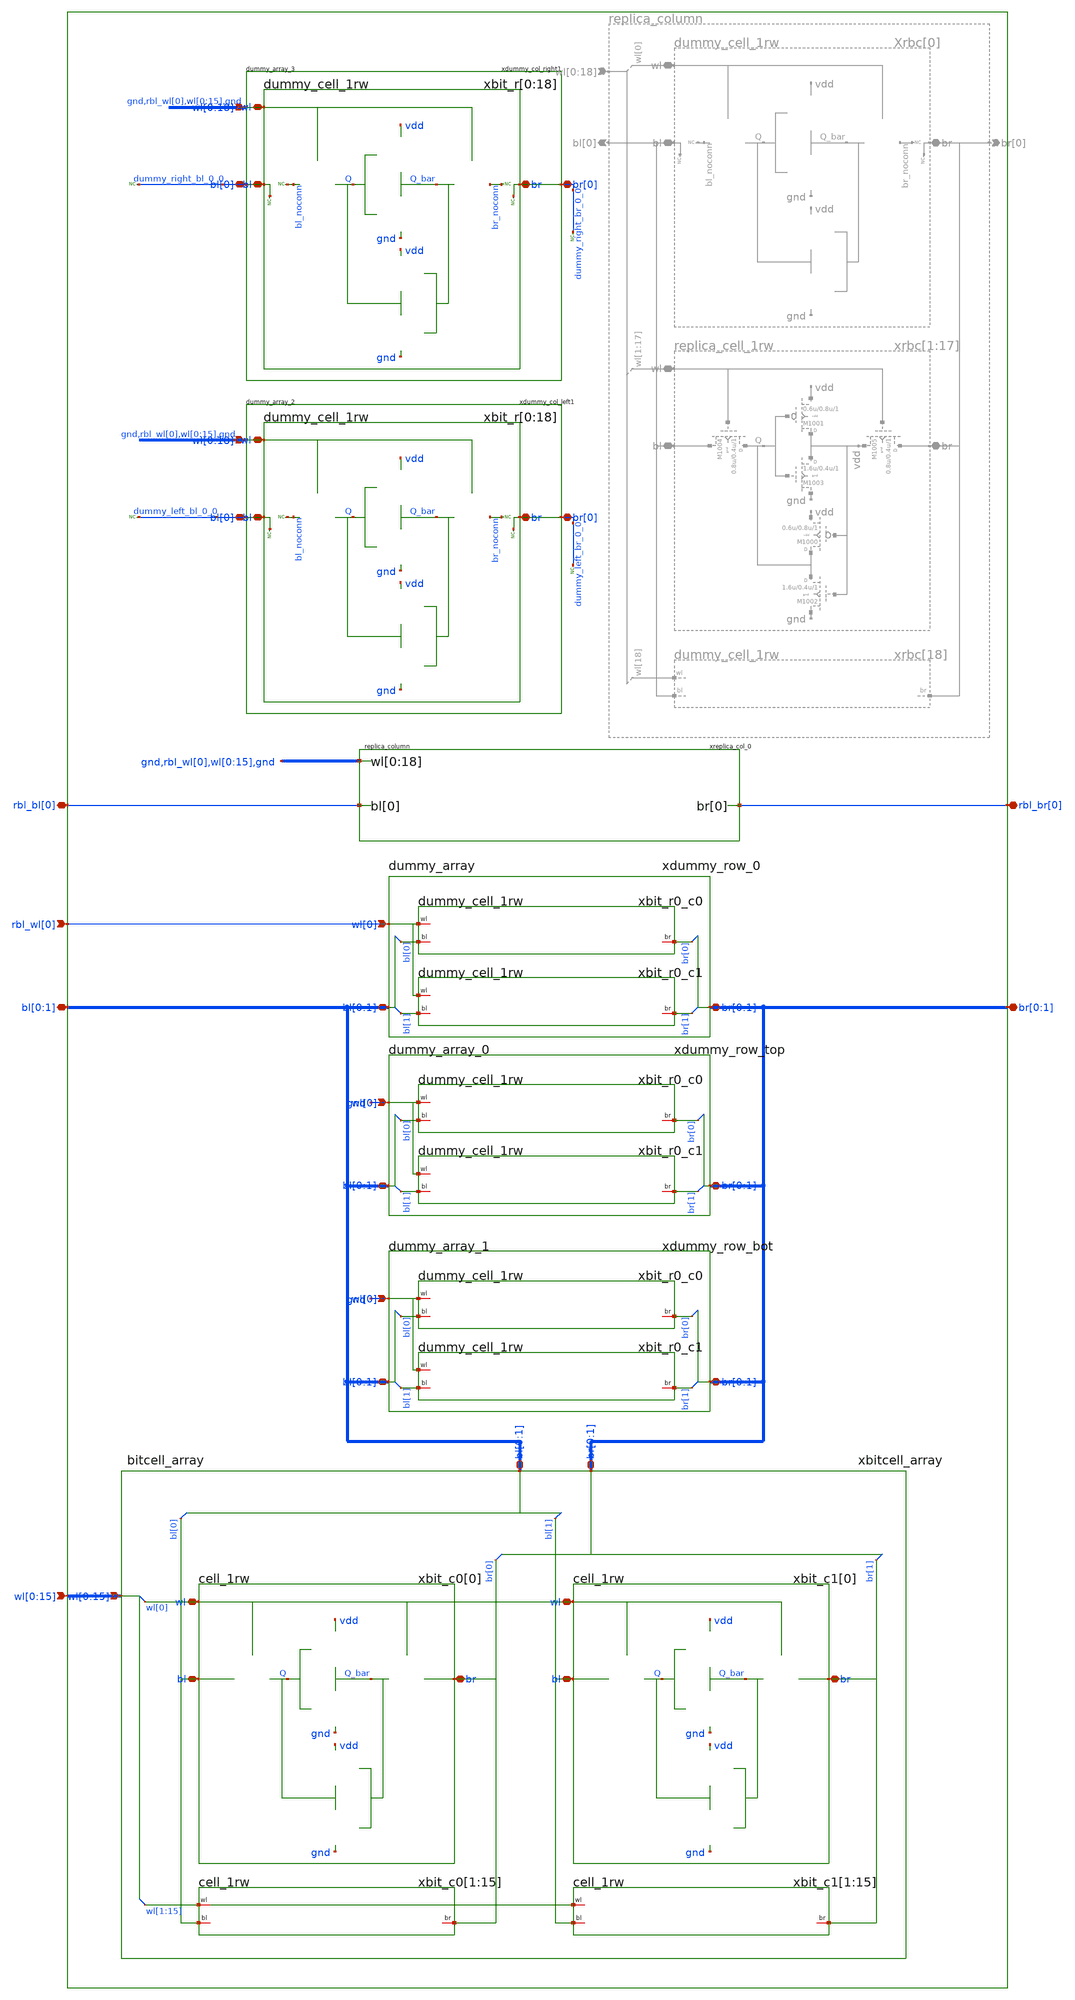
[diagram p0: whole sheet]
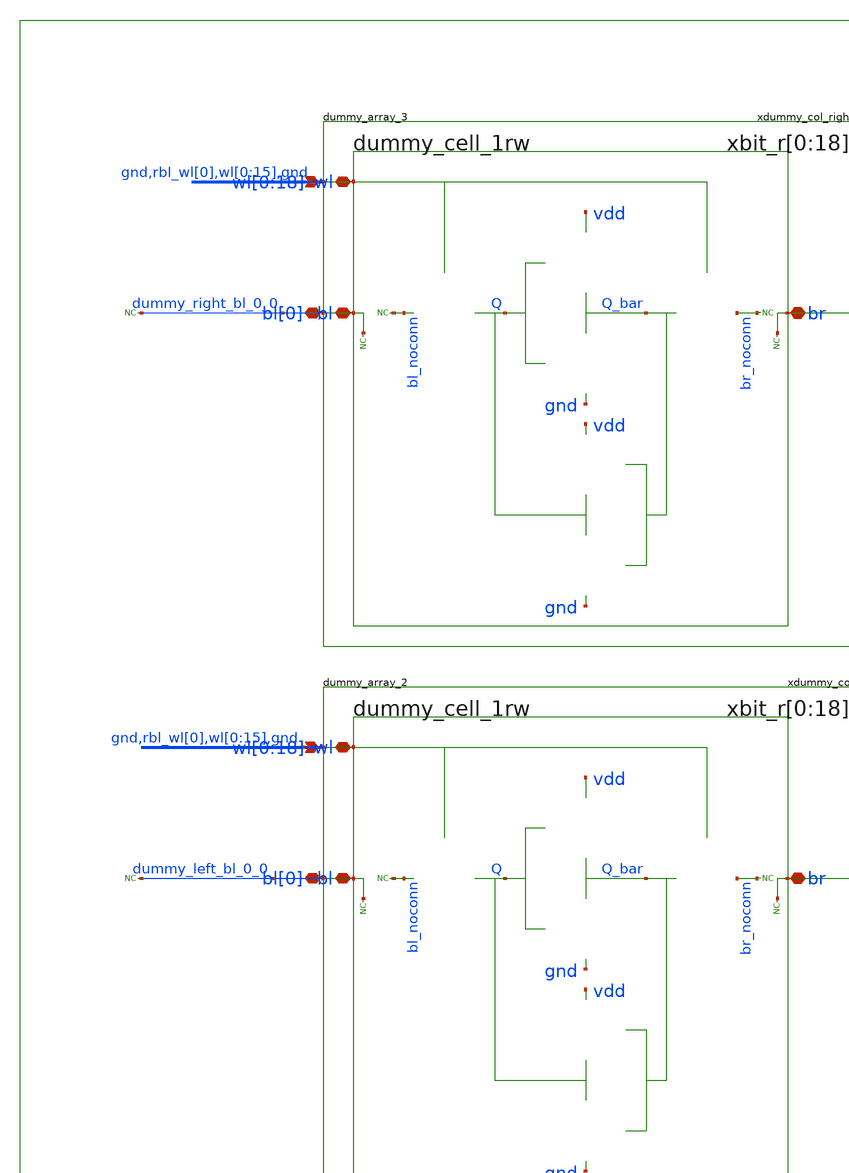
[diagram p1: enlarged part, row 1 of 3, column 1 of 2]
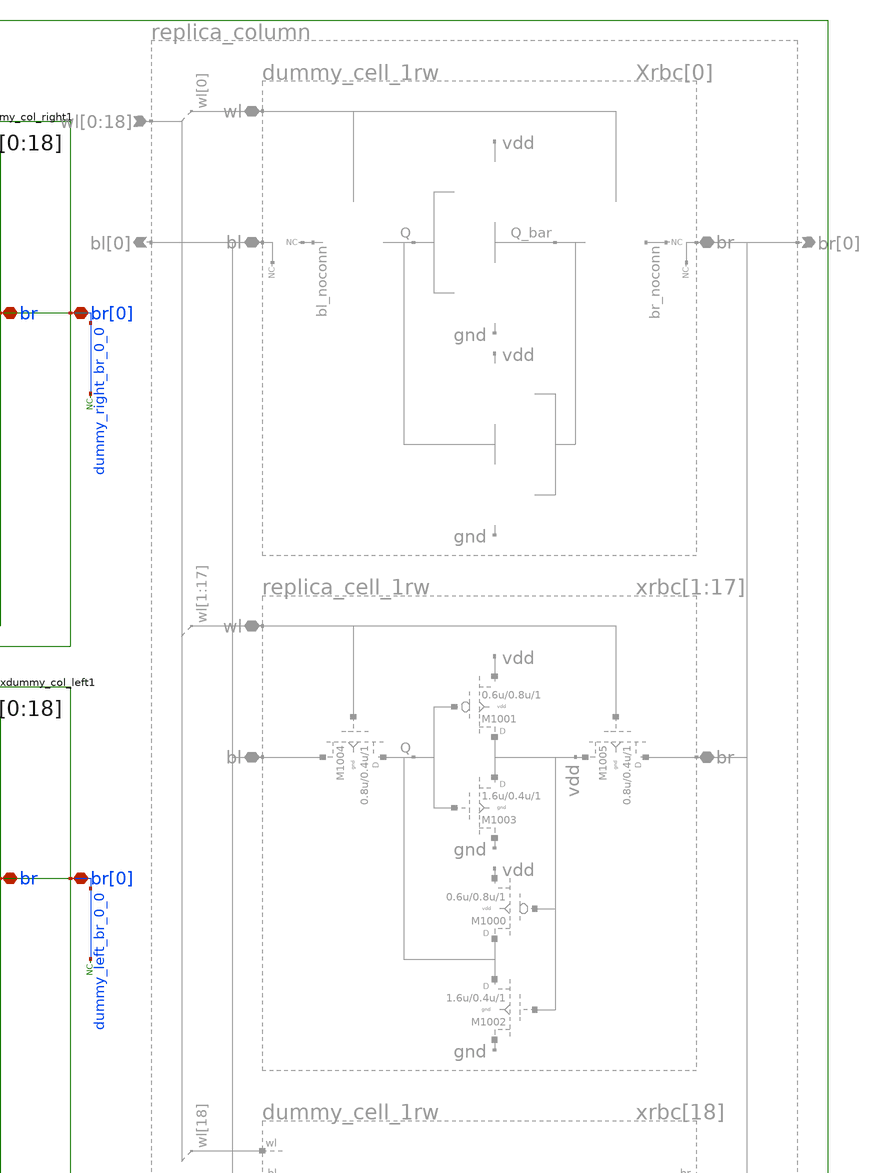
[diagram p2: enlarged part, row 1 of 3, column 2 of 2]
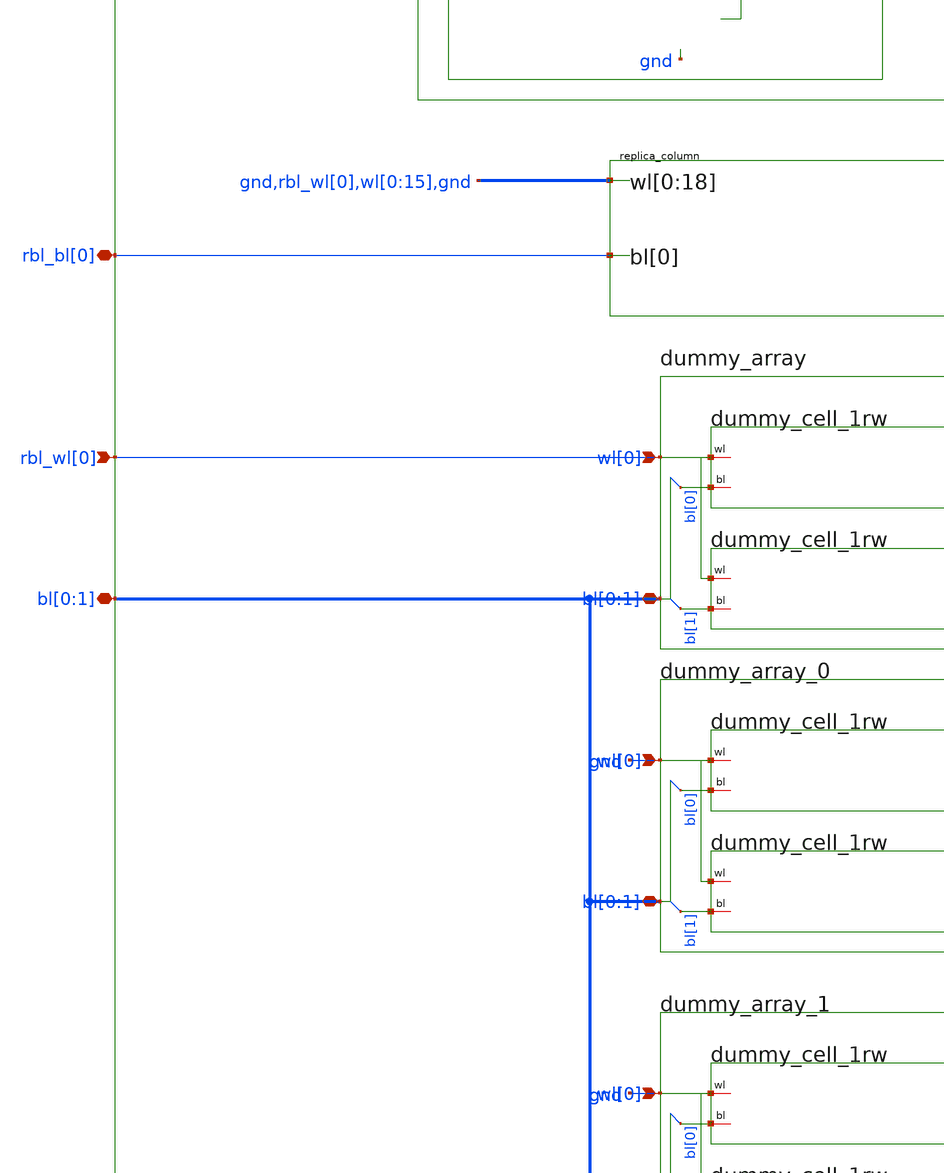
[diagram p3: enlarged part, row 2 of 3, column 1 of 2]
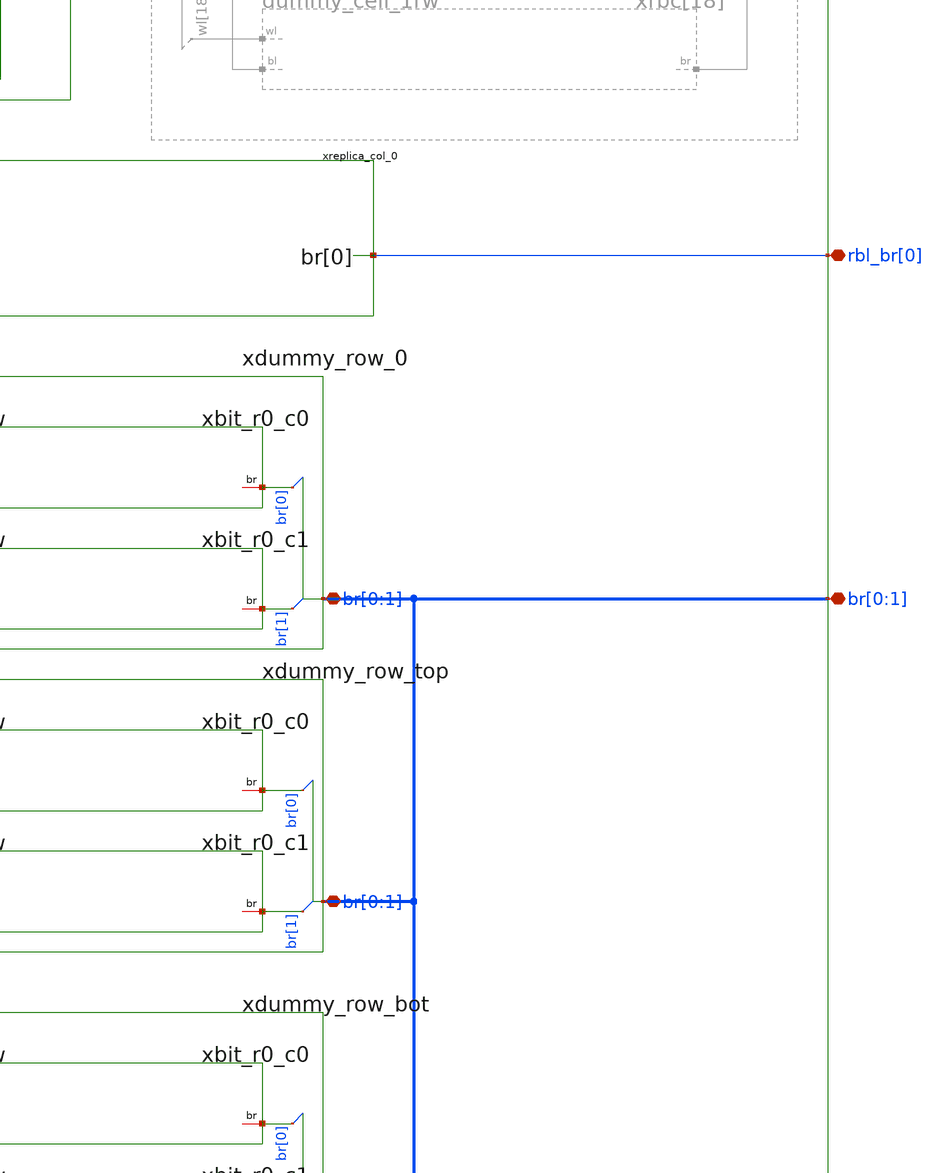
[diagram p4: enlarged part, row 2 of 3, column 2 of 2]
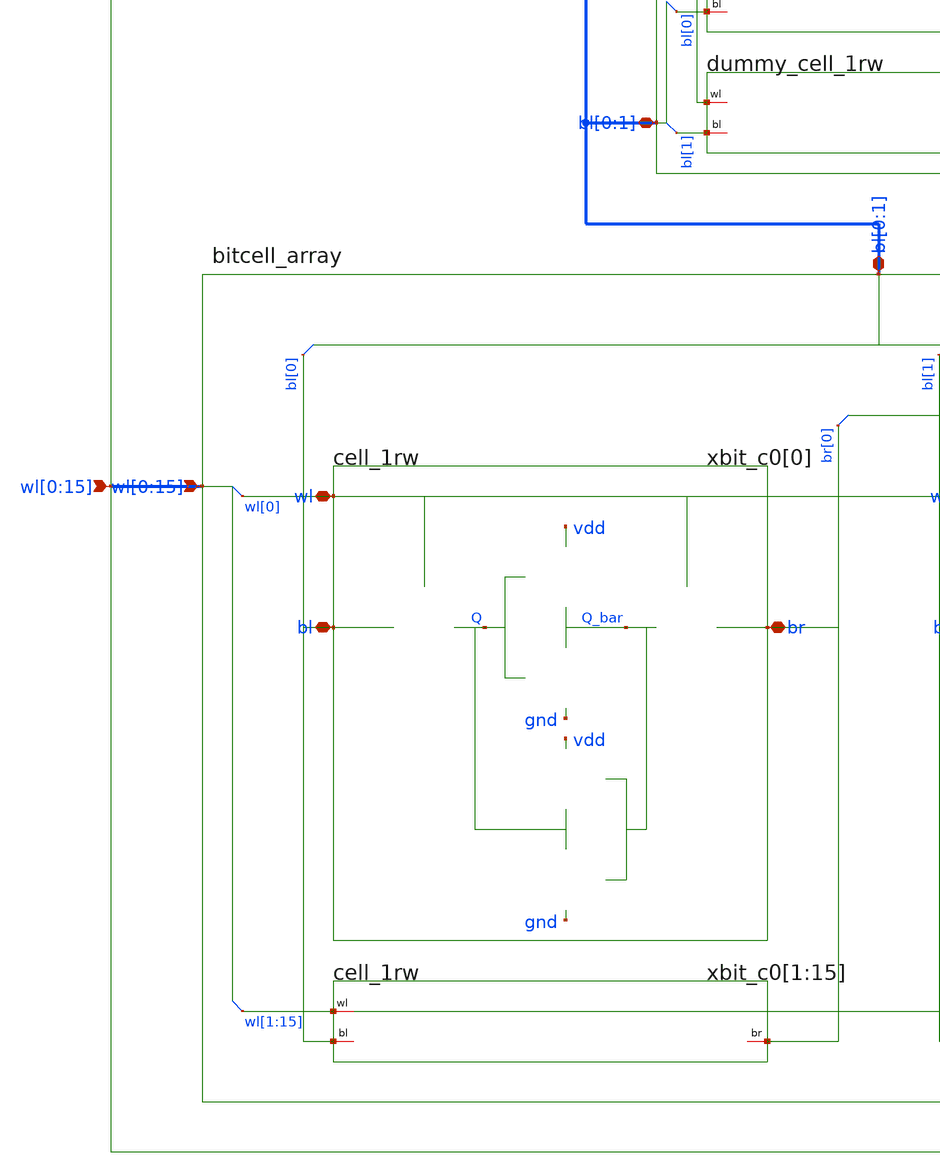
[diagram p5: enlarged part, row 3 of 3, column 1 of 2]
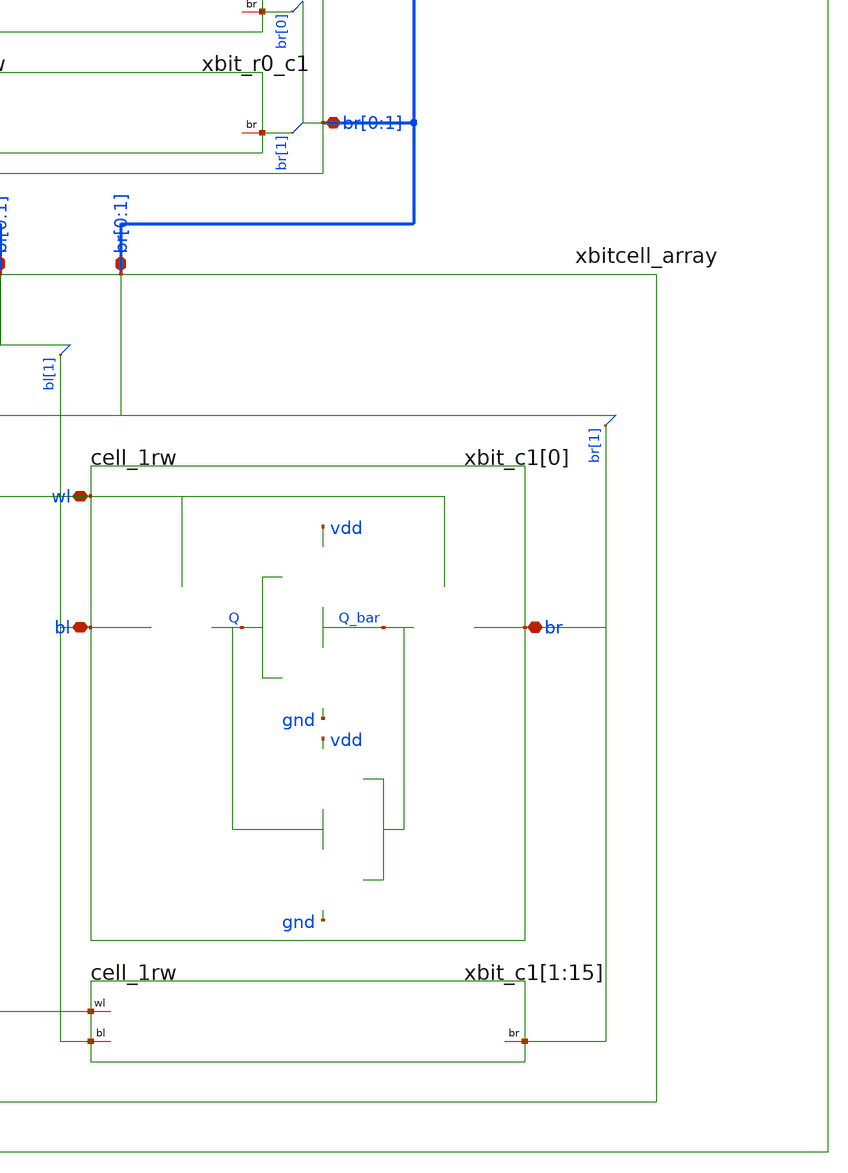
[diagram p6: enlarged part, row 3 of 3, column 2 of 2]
** sch_path: sram_2_16_scn4m/replica_bitcell_array.sch
**.subckt replica_bitcell_array rbl_bl[0] rbl_br[0] bl[0],bl[1] br[0],br[1] rbl_wl[0]
*+ wl[0],wl[1],wl[2],wl[3],wl[4],wl[5],wl[6],wl[7],wl[8],wl[9],wl[10],wl[11],wl[12],wl[13],wl[14],wl[15]
*.iopin rbl_bl[0]
*.iopin rbl_br[0]
*.iopin bl[0],bl[1]
*.iopin br[0],br[1]
*.ipin rbl_wl[0]
*.ipin
*+ wl[0],wl[1],wl[2],wl[3],wl[4],wl[5],wl[6],wl[7],wl[8],wl[9],wl[10],wl[11],wl[12],wl[13],wl[14],wl[15]
xreplica_col_0 rbl_bl[0] rbl_br[0] gnd rbl_wl[0] wl[0] wl[1] wl[2] wl[3] wl[4] wl[5] wl[6] wl[7]
+ wl[8] wl[9] wl[10] wl[11] wl[12] wl[13] wl[14] wl[15] gnd vdd gnd replica_column
xbitcell_array bl[0] bl[1] br[0] br[1] wl[0] wl[1] wl[2] wl[3] wl[4] wl[5] wl[6] wl[7] wl[8] wl[9]
+ wl[10] wl[11] wl[12] wl[13] wl[14] wl[15] vdd gnd bitcell_array
xdummy_row_top bl[0] bl[1] br[0] br[1] gnd vdd gnd dummy_array_1
xdummy_row_0 bl[0] bl[1] br[0] br[1] rbl_wl[0] vdd gnd dummy_array
xdummy_col_left1 dummy_left_bl_0_0 dummy_left_br_0_0 gnd rbl_wl[0] wl[0] wl[1] wl[2] wl[3] wl[4]
+ wl[5] wl[6] wl[7] wl[8] wl[9] wl[10] wl[11] wl[12] wl[13] wl[14] wl[15] gnd vdd gnd dummy_array_2
xdummy_col_right1 dummy_right_bl_0_0 dummy_right_br_0_0 gnd rbl_wl[0] wl[0] wl[1] wl[2] wl[3] wl[4]
+ wl[5] wl[6] wl[7] wl[8] wl[9] wl[10] wl[11] wl[12] wl[13] wl[14] wl[15] gnd vdd gnd dummy_array_3
* noconn dummy_right_bl_0_0
* noconn dummy_right_br_0_0
* noconn dummy_left_bl_0_0
* noconn dummy_left_br_0_0
xdummy_row_bot bl[0] bl[1] br[0] br[1] gnd vdd gnd dummy_array_0
**.ends
.end
